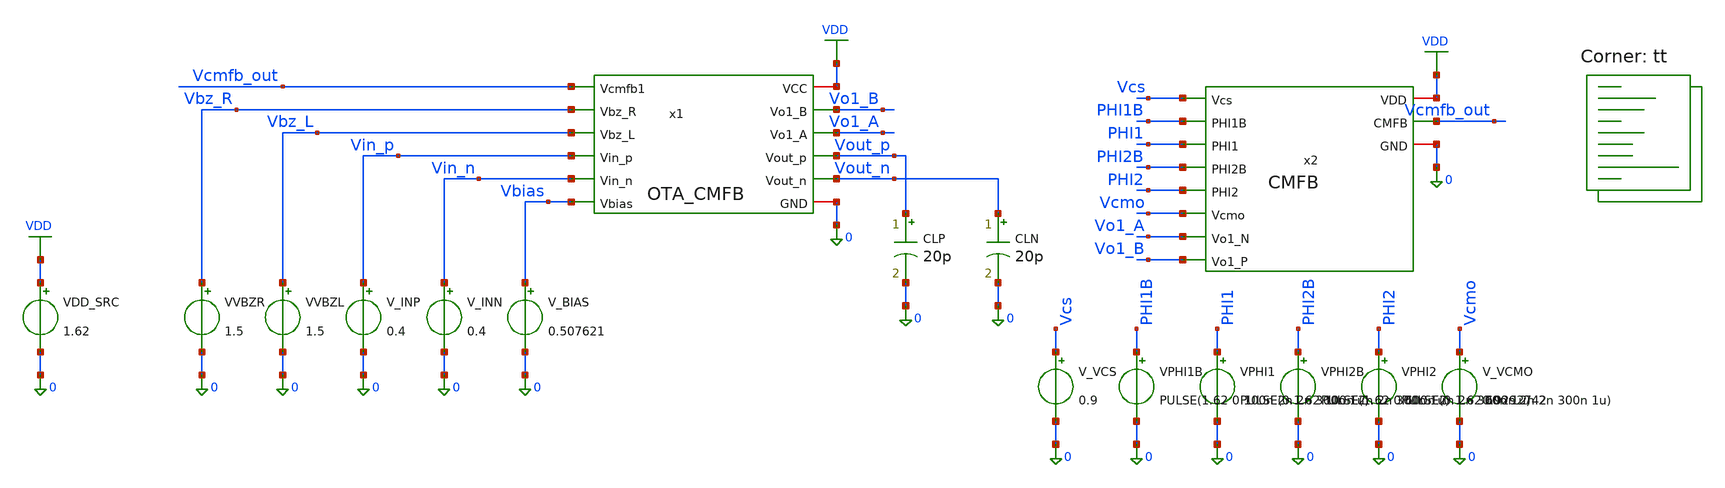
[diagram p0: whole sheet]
** sch_path: blocks/02_CMFB/sim/tb_CMFB_PVT_04_TT_1v62_27C.sch
**.subckt tb_CMFB_PVT_04_TT_1v62_27C
x1 VDD Vcmfb_out Vbz_R Vbz_L Vin_p Vin_n Vo1_B Vo1_A Vout_p Vout_n Vbias 0 OTA_CMFB
x2 Vcmfb_out Vcs PHI1B PHI1 VDD PHI2B 0 PHI2 Vcmo Vo1_A Vo1_B CMFB
VDD_SRC VDD 0 1.62
VVBZR Vbz_R 0 1.5
VVBZL Vbz_L 0 1.5
V_INP Vin_p 0 0.4
V_INN Vin_n 0 0.4
V_BIAS Vbias 0 0.507621
CLP Vout_p 0 20p m=1
CLN Vout_n 0 20p m=1
V_VCS Vcs 0 0.9
VPHI1B PHI1B 0 PULSE(1.62 0 100n 2n 2n 300n 1u)
VPHI1 PHI1 0 PULSE(0 1.62 100n 2n 2n 300n 1u)
VPHI2B PHI2B 0 PULSE(1.62 0 600n 2n 2n 300n 1u)
VPHI2 PHI2 0 PULSE(0 1.62 600n 2n 2n 300n 1u)
V_VCMO Vcmo 0 0.9292742
**** begin user architecture code
.lib $::SKYWATER_MODELS/sky130.lib.spice tt


* OTA_CMFB + SC_CMFB PVT SCREENING
* fixed independent bias references, with VDD-tracking clock amplitude
* Observe period averages/ripple/drift, do not declare PVT pass by convergence alone.
.temp 27
.options rshunt=1e12
RLEAK_CMFB Vcmfb_out 0 1e12
.control
save all
tran 1n 100u
let vo1cm = (v(vo1_a)+v(vo1_b))/2
let vo1d = v(vo1_a)-v(vo1_b)
let vocm = (v(vout_p)+v(vout_n))/2
let vod = v(vout_p)-v(vout_n)
meas tran VO1CM_LAST AVG vo1cm FROM=90u TO=100u
meas tran VO1CM_MIN MIN vo1cm FROM=90u TO=100u
meas tran VO1CM_MAX MAX vo1cm FROM=90u TO=100u
meas tran VO1CM_PREV AVG vo1cm FROM=80u TO=90u
meas tran CMFB_LAST AVG v(vcmfb_out) FROM=90u TO=100u
meas tran CMFB_MIN MIN v(vcmfb_out) FROM=90u TO=100u
meas tran CMFB_MAX MAX v(vcmfb_out) FROM=90u TO=100u
meas tran CMFB_PREV AVG v(vcmfb_out) FROM=80u TO=90u
meas tran VOUTCM_LAST AVG vocm FROM=90u TO=100u
meas tran VOUTCM_PREV AVG vocm FROM=80u TO=90u
meas tran VOUTCM_MIN MIN vocm FROM=90u TO=100u
meas tran VOUTCM_MAX MAX vocm FROM=90u TO=100u
meas tran VOD_LAST AVG vod FROM=90u TO=100u
meas tran VO1D_LAST AVG vo1d FROM=90u TO=100u
meas tran PHI1_MAX MAX v(phi1) FROM=90u TO=100u
meas tran PHI1_MIN MIN v(phi1) FROM=90u TO=100u
meas tran PHI2_MAX MAX v(phi2) FROM=90u TO=100u
meas tran PHI2_MIN MIN v(phi2) FROM=90u TO=100u
let VO1CM_ERR = VO1CM_LAST-0.9292742
let VO1CM_RIPPLE = VO1CM_MAX-VO1CM_MIN
let CMFB_RIPPLE = CMFB_MAX-CMFB_MIN
let VOUTCM_RIPPLE = VOUTCM_MAX-VOUTCM_MIN
let CM_DRIFT = VO1CM_LAST-VO1CM_PREV
let CTRL_DRIFT = CMFB_LAST-CMFB_PREV
let OUT_DRIFT = VOUTCM_LAST-VOUTCM_PREV
echo ========= OTA CLOSED LOOP PVT SCREEN =========
print VO1CM_LAST VO1CM_ERR VO1CM_RIPPLE
print CMFB_LAST CMFB_MIN CMFB_MAX CMFB_RIPPLE
print VOUTCM_LAST VOUTCM_RIPPLE VOD_LAST VO1D_LAST
print CM_DRIFT CTRL_DRIFT OUT_DRIFT
print PHI1_MAX PHI1_MIN PHI2_MAX PHI2_MIN
plot vo1cm
plot v(vcmfb_out)
.endc


**** end user architecture code
**.ends
.GLOBAL VDD
.end
